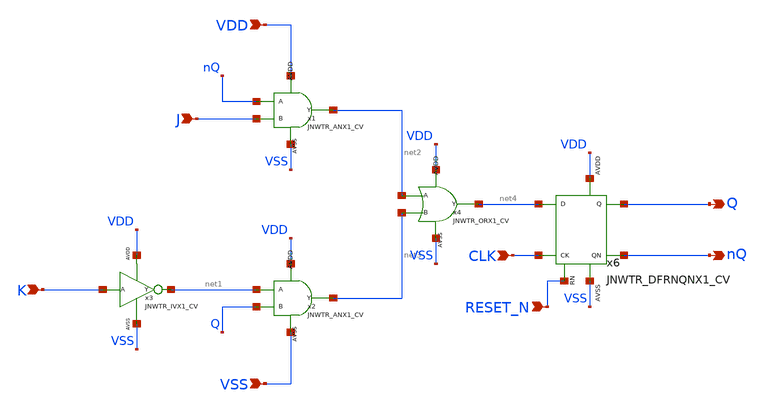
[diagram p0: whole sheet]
** sch_path: design/JNW_GR05_SKY130A/JKflipflop.sch
**.subckt JKflipflop J K CLK VDD VSS nQ Q RESET_N
*.ipin J
*.ipin K
*.ipin CLK
*.ipin VDD
*.ipin VSS
*.opin nQ
*.opin Q
*.ipin RESET_N
x1 nQ J net2 VDD VSS JNWTR_ANX1_CV xoffset=0 yoffset=0 angle=0 M=1
x2 net1 Q net3 VDD VSS JNWTR_ANX1_CV xoffset=0 yoffset=0 angle=0 M=1
x3 K net1 VDD VSS JNWTR_IVX1_CV
x4 net2 net3 net4 VDD VSS JNWTR_ORX1_CV xoffset=0 yoffset=0 angle=0 M=1
x6 net4 CLK RESET_N Q nQ VDD VSS JNWTR_DFRNQNX1_CV xoffset=0 yoffset=0 angle=0
**.ends
.end
